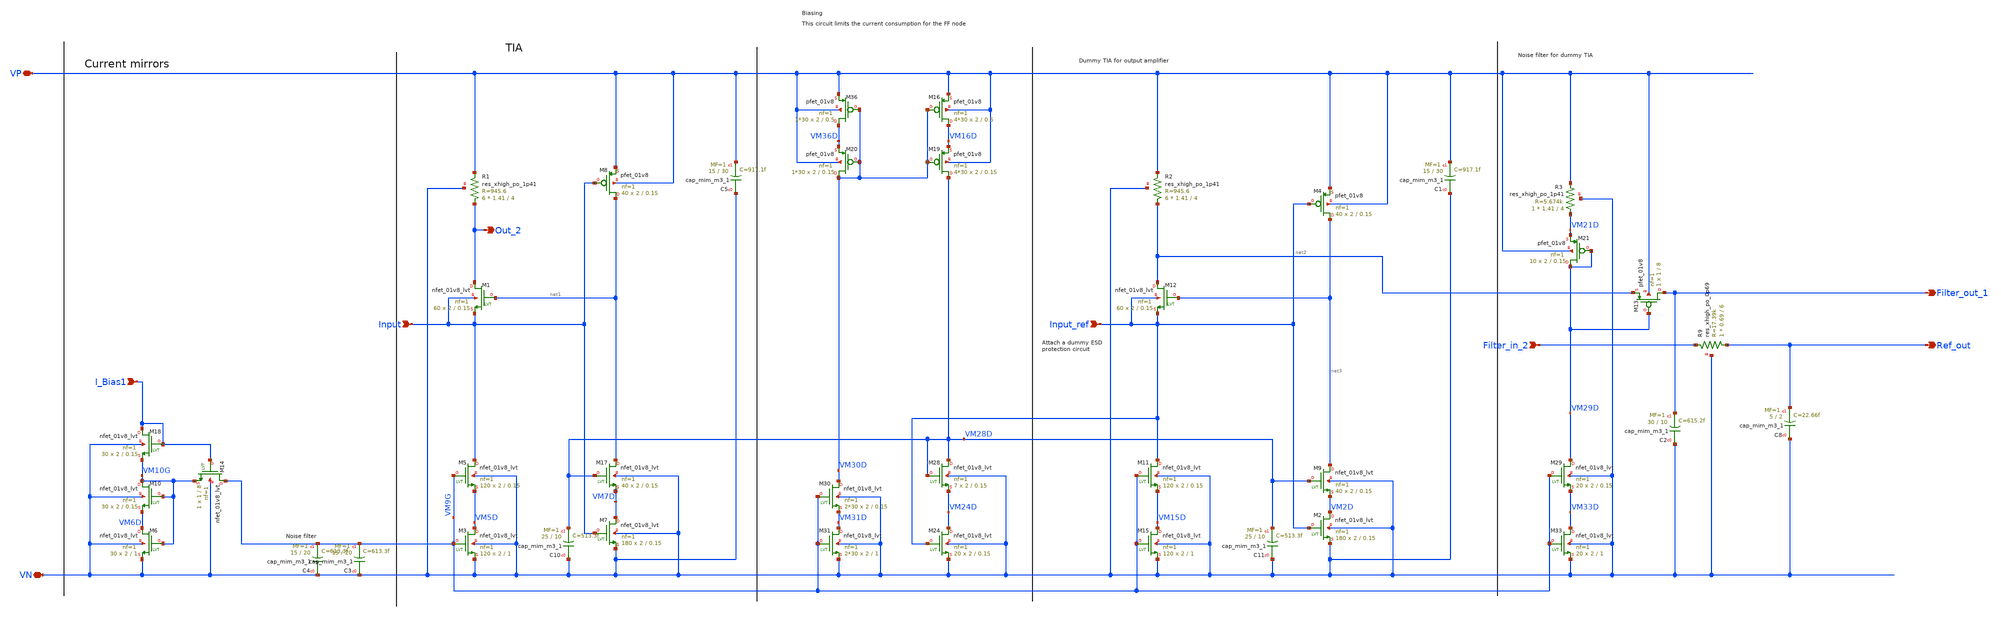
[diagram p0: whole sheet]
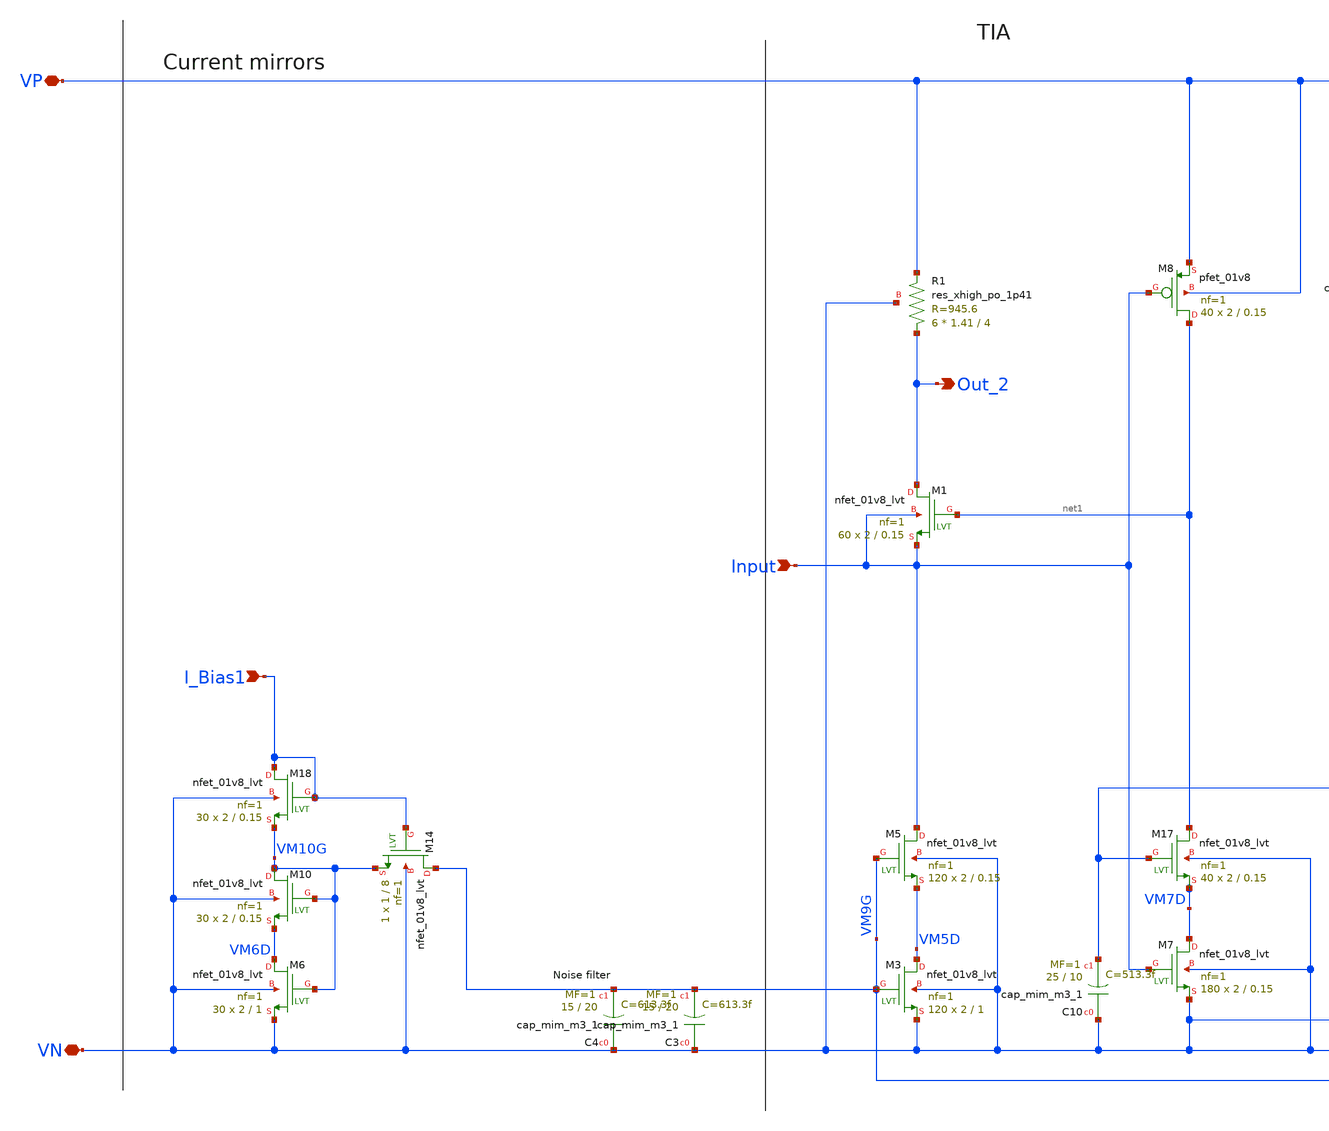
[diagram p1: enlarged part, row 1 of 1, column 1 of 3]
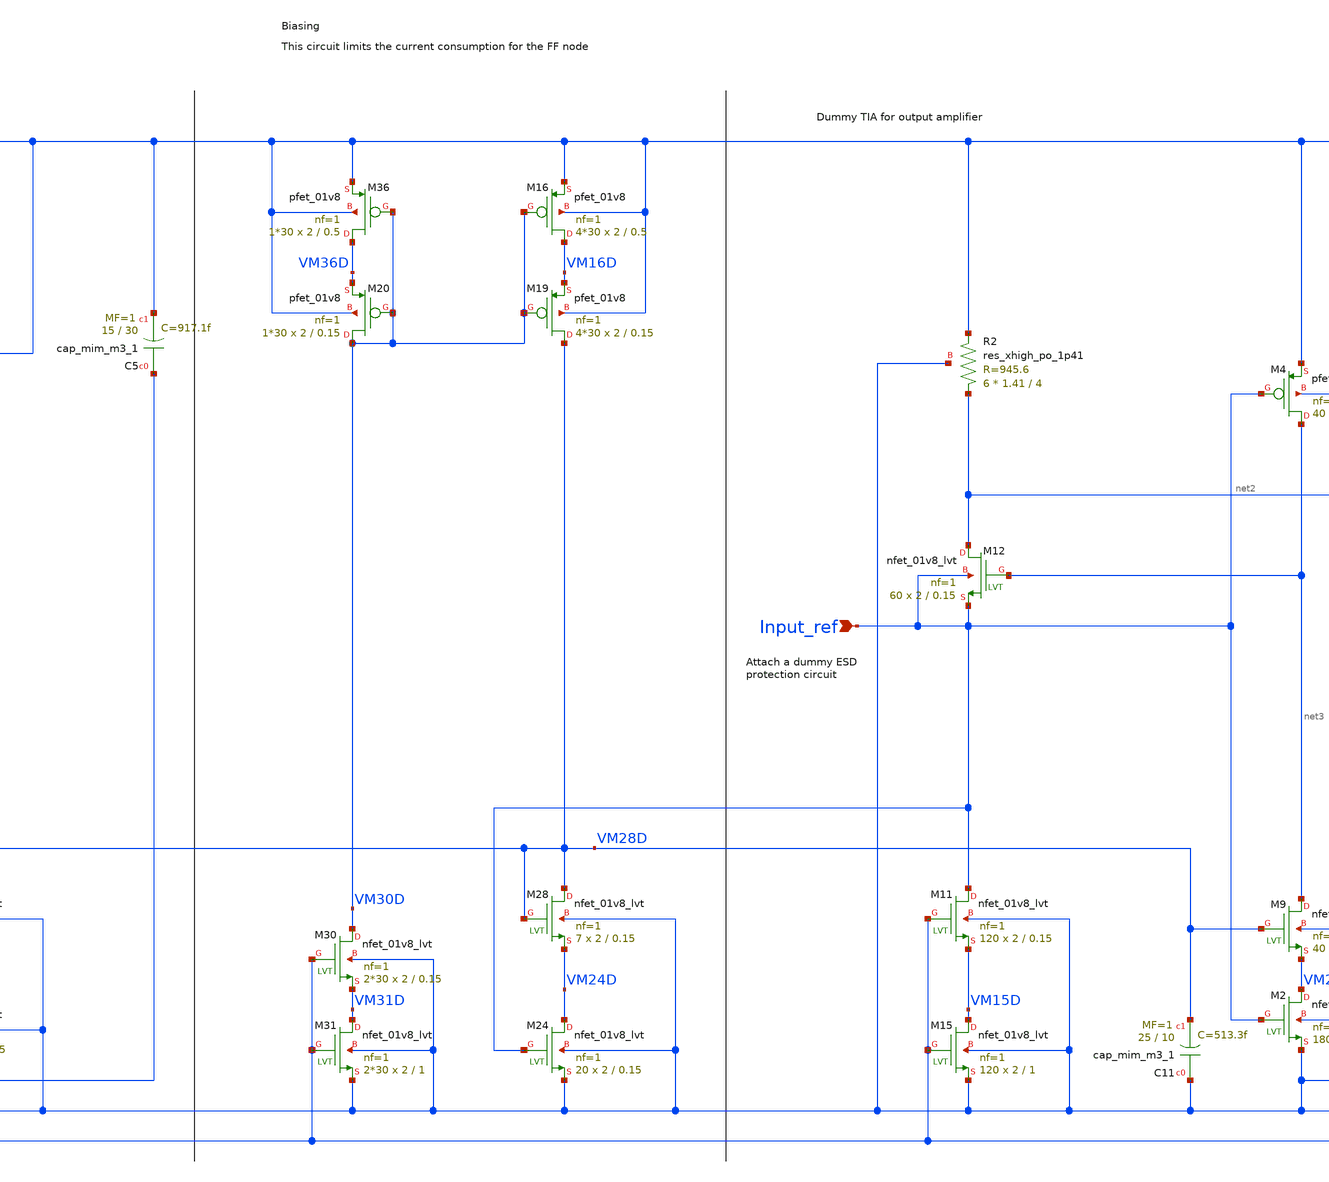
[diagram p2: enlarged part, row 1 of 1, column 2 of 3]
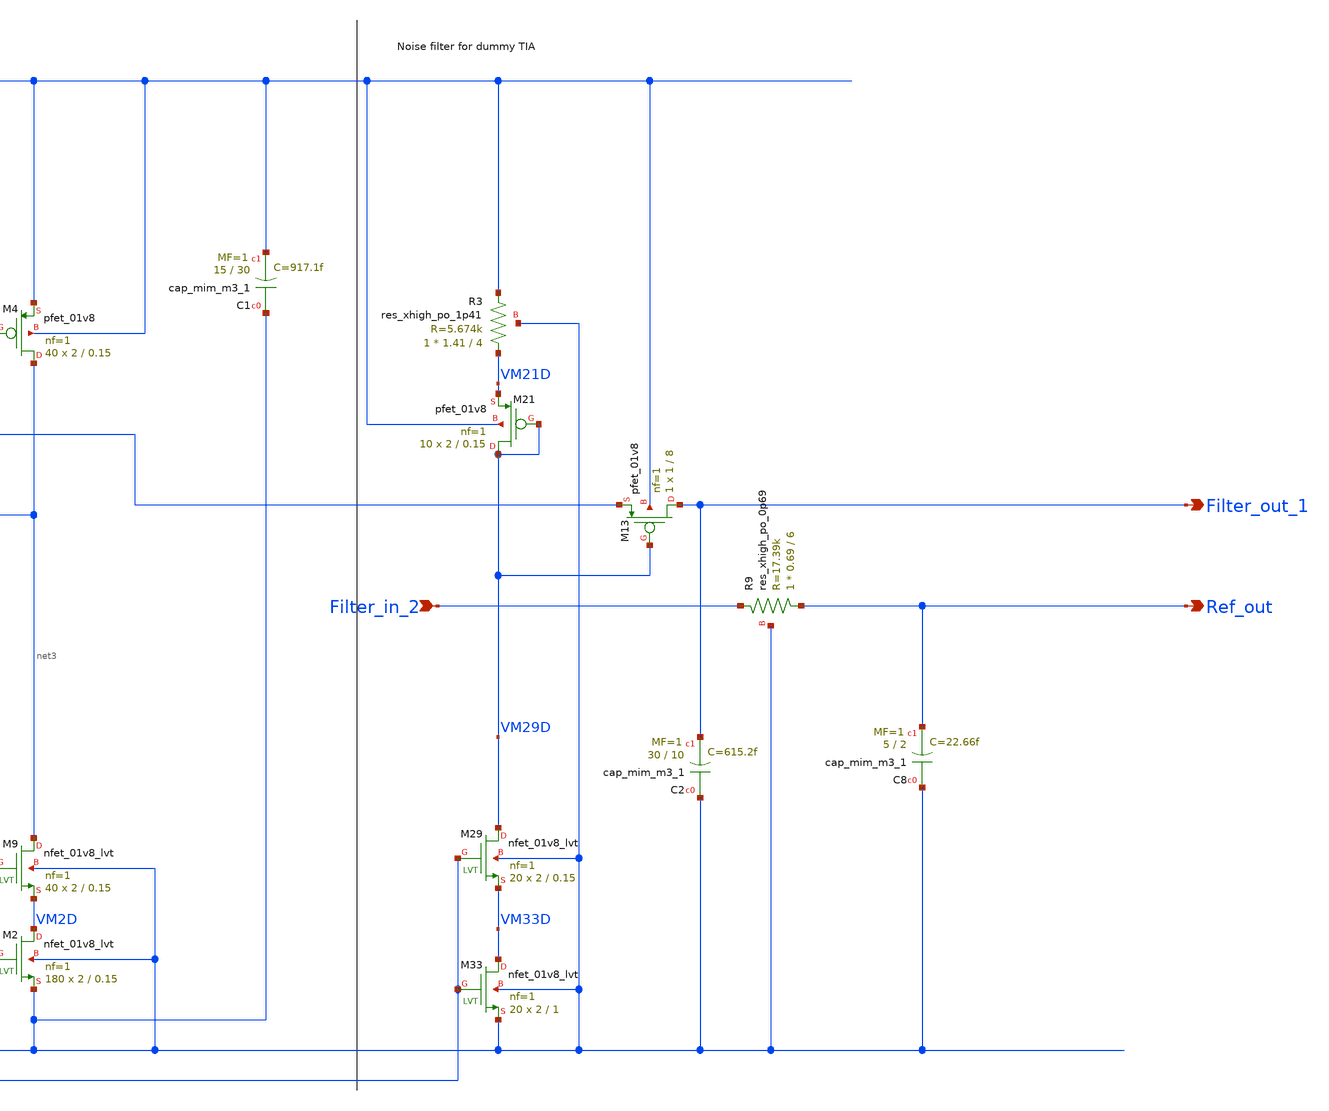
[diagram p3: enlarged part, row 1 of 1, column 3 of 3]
** sch_path: xschem/tia/tiaA.sch
**.subckt tiaA VN VP Out_2 I_Bias1 Input Input_ref Filter_out_1 Filter_in_2 Ref_out
*.iopin VN
*.iopin VP
*.opin Out_2
*.ipin I_Bias1
*.ipin Input
*.ipin Input_ref
*.opin Filter_out_1
*.ipin Filter_in_2
*.opin Ref_out
XM7 VM7D Input VN VN sky130_fd_pr__nfet_01v8_lvt L=0.15 W=2 nf=1 ad='int((nf+1)/2) * W/nf * 0.29' as='int((nf+2)/2) * W/nf * 0.29'
+ pd='2*int((nf+1)/2) * (W/nf + 0.29)' ps='2*int((nf+2)/2) * (W/nf + 0.29)' nrd='0.29 / W' nrs='0.29 / W'
+ sa=0 sb=0 sd=0 mult=180 m=180
XM8 net1 Input VP VP sky130_fd_pr__pfet_01v8 L=0.15 W=2 nf=1 ad='int((nf+1)/2) * W/nf * 0.29' as='int((nf+2)/2) * W/nf * 0.29'
+ pd='2*int((nf+1)/2) * (W/nf + 0.29)' ps='2*int((nf+2)/2) * (W/nf + 0.29)' nrd='0.29 / W' nrs='0.29 / W'
+ sa=0 sb=0 sd=0 mult=40 m=40
XC4 VN VM9G sky130_fd_pr__cap_mim_m3_1 W=15 L=20 MF=1 m=1
XM18 I_Bias1 I_Bias1 VM10G VN sky130_fd_pr__nfet_01v8_lvt L=0.15 W=2 nf=1 ad='int((nf+1)/2) * W/nf * 0.29'
+ as='int((nf+2)/2) * W/nf * 0.29' pd='2*int((nf+1)/2) * (W/nf + 0.29)' ps='2*int((nf+2)/2) * (W/nf + 0.29)'
+ nrd='0.29 / W' nrs='0.29 / W' sa=0 sb=0 sd=0 mult=30 m=30
XM10 VM10G VM10G VM6D VN sky130_fd_pr__nfet_01v8_lvt L=0.15 W=2 nf=1 ad='int((nf+1)/2) * W/nf * 0.29'
+ as='int((nf+2)/2) * W/nf * 0.29' pd='2*int((nf+1)/2) * (W/nf + 0.29)' ps='2*int((nf+2)/2) * (W/nf + 0.29)'
+ nrd='0.29 / W' nrs='0.29 / W' sa=0 sb=0 sd=0 mult=30 m=30
XM5 Input VM9G VM5D VN sky130_fd_pr__nfet_01v8_lvt L=0.15 W=2 nf=1 ad='int((nf+1)/2) * W/nf * 0.29' as='int((nf+2)/2) * W/nf * 0.29'
+ pd='2*int((nf+1)/2) * (W/nf + 0.29)' ps='2*int((nf+2)/2) * (W/nf + 0.29)' nrd='0.29 / W' nrs='0.29 / W'
+ sa=0 sb=0 sd=0 mult=120 m=120
XM6 VM6D VM10G VN VN sky130_fd_pr__nfet_01v8_lvt L=1 W=2 nf=1 ad='int((nf+1)/2) * W/nf * 0.29' as='int((nf+2)/2) * W/nf * 0.29'
+ pd='2*int((nf+1)/2) * (W/nf + 0.29)' ps='2*int((nf+2)/2) * (W/nf + 0.29)' nrd='0.29 / W' nrs='0.29 / W'
+ sa=0 sb=0 sd=0 mult=30 m=30
XM14 VM9G I_Bias1 VM10G VN sky130_fd_pr__nfet_01v8_lvt L=8 W=1 nf=1 ad='int((nf+1)/2) * W/nf * 0.29'
+ as='int((nf+2)/2) * W/nf * 0.29' pd='2*int((nf+1)/2) * (W/nf + 0.29)' ps='2*int((nf+2)/2) * (W/nf + 0.29)'
+ nrd='0.29 / W' nrs='0.29 / W' sa=0 sb=0 sd=0 mult=1 m=1
XM1 Out_2 net1 Input Input sky130_fd_pr__nfet_01v8_lvt L=0.15 W=2 nf=1 ad='int((nf+1)/2) * W/nf * 0.29'
+ as='int((nf+2)/2) * W/nf * 0.29' pd='2*int((nf+1)/2) * (W/nf + 0.29)' ps='2*int((nf+2)/2) * (W/nf + 0.29)'
+ nrd='0.29 / W' nrs='0.29 / W' sa=0 sb=0 sd=0 mult=60 m=60
XM3 VM5D VM9G VN VN sky130_fd_pr__nfet_01v8_lvt L=1 W=2 nf=1 ad='int((nf+1)/2) * W/nf * 0.29' as='int((nf+2)/2) * W/nf * 0.29'
+ pd='2*int((nf+1)/2) * (W/nf + 0.29)' ps='2*int((nf+2)/2) * (W/nf + 0.29)' nrd='0.29 / W' nrs='0.29 / W'
+ sa=0 sb=0 sd=0 mult=120 m=120
XR1 Out_2 VP VN sky130_fd_pr__res_xhigh_po_1p41 L=4 mult=6 m=6
XM2 VM2D Input_ref VN VN sky130_fd_pr__nfet_01v8_lvt L=0.15 W=2 nf=1 ad='int((nf+1)/2) * W/nf * 0.29'
+ as='int((nf+2)/2) * W/nf * 0.29' pd='2*int((nf+1)/2) * (W/nf + 0.29)' ps='2*int((nf+2)/2) * (W/nf + 0.29)'
+ nrd='0.29 / W' nrs='0.29 / W' sa=0 sb=0 sd=0 mult=180 m=180
XM4 net3 Input_ref VP VP sky130_fd_pr__pfet_01v8 L=0.15 W=2 nf=1 ad='int((nf+1)/2) * W/nf * 0.29' as='int((nf+2)/2) * W/nf * 0.29'
+ pd='2*int((nf+1)/2) * (W/nf + 0.29)' ps='2*int((nf+2)/2) * (W/nf + 0.29)' nrd='0.29 / W' nrs='0.29 / W'
+ sa=0 sb=0 sd=0 mult=40 m=40
XM11 Input_ref VM9G VM15D VN sky130_fd_pr__nfet_01v8_lvt L=0.15 W=2 nf=1 ad='int((nf+1)/2) * W/nf * 0.29'
+ as='int((nf+2)/2) * W/nf * 0.29' pd='2*int((nf+1)/2) * (W/nf + 0.29)' ps='2*int((nf+2)/2) * (W/nf + 0.29)'
+ nrd='0.29 / W' nrs='0.29 / W' sa=0 sb=0 sd=0 mult=120 m=120
XM12 net2 net3 Input_ref Input_ref sky130_fd_pr__nfet_01v8_lvt L=0.15 W=2 nf=1 ad='int((nf+1)/2) * W/nf * 0.29'
+ as='int((nf+2)/2) * W/nf * 0.29' pd='2*int((nf+1)/2) * (W/nf + 0.29)' ps='2*int((nf+2)/2) * (W/nf + 0.29)'
+ nrd='0.29 / W' nrs='0.29 / W' sa=0 sb=0 sd=0 mult=60 m=60
XM15 VM15D VM9G VN VN sky130_fd_pr__nfet_01v8_lvt L=1 W=2 nf=1 ad='int((nf+1)/2) * W/nf * 0.29' as='int((nf+2)/2) * W/nf * 0.29'
+ pd='2*int((nf+1)/2) * (W/nf + 0.29)' ps='2*int((nf+2)/2) * (W/nf + 0.29)' nrd='0.29 / W' nrs='0.29 / W'
+ sa=0 sb=0 sd=0 mult=120 m=120
XR2 net2 VP VN sky130_fd_pr__res_xhigh_po_1p41 L=4 mult=6 m=6
XC5 VN VP sky130_fd_pr__cap_mim_m3_1 W=15 L=30 MF=1 m=1
XC1 VN VP sky130_fd_pr__cap_mim_m3_1 W=15 L=30 MF=1 m=1
XC2 VN Filter_out_1 sky130_fd_pr__cap_mim_m3_1 W=30 L=10 MF=1 m=1
XM29 VM29D VM9G VM33D VN sky130_fd_pr__nfet_01v8_lvt L=0.15 W=2 nf=1 ad='int((nf+1)/2) * W/nf * 0.29'
+ as='int((nf+2)/2) * W/nf * 0.29' pd='2*int((nf+1)/2) * (W/nf + 0.29)' ps='2*int((nf+2)/2) * (W/nf + 0.29)'
+ nrd='0.29 / W' nrs='0.29 / W' sa=0 sb=0 sd=0 mult=20 m=20
XM33 VM33D VM9G VN VN sky130_fd_pr__nfet_01v8_lvt L=1 W=2 nf=1 ad='int((nf+1)/2) * W/nf * 0.29' as='int((nf+2)/2) * W/nf * 0.29'
+ pd='2*int((nf+1)/2) * (W/nf + 0.29)' ps='2*int((nf+2)/2) * (W/nf + 0.29)' nrd='0.29 / W' nrs='0.29 / W'
+ sa=0 sb=0 sd=0 mult=20 m=20
XR3 VM21D VP VN sky130_fd_pr__res_xhigh_po_1p41 L=4 mult=1 m=1
XM21 VM29D VM29D VM21D VP sky130_fd_pr__pfet_01v8 L=0.15 W=2 nf=1 ad='int((nf+1)/2) * W/nf * 0.29' as='int((nf+2)/2) * W/nf * 0.29'
+ pd='2*int((nf+1)/2) * (W/nf + 0.29)' ps='2*int((nf+2)/2) * (W/nf + 0.29)' nrd='0.29 / W' nrs='0.29 / W'
+ sa=0 sb=0 sd=0 mult=10 m=10
XM13 Filter_out_1 VM29D net2 VP sky130_fd_pr__pfet_01v8 L=8 W=1 nf=1 ad='int((nf+1)/2) * W/nf * 0.29'
+ as='int((nf+2)/2) * W/nf * 0.29' pd='2*int((nf+1)/2) * (W/nf + 0.29)' ps='2*int((nf+2)/2) * (W/nf + 0.29)'
+ nrd='0.29 / W' nrs='0.29 / W' sa=0 sb=0 sd=0 mult=1 m=1
XM24 VM24D Input_ref VN VN sky130_fd_pr__nfet_01v8_lvt L=0.15 W=2 nf=1 ad='int((nf+1)/2) * W/nf * 0.29'
+ as='int((nf+2)/2) * W/nf * 0.29' pd='2*int((nf+1)/2) * (W/nf + 0.29)' ps='2*int((nf+2)/2) * (W/nf + 0.29)'
+ nrd='0.29 / W' nrs='0.29 / W' sa=0 sb=0 sd=0 mult=20 m=20
XM30 VM30D VM9G VM31D VN sky130_fd_pr__nfet_01v8_lvt L=0.15 W=2 nf=1 ad='int((nf+1)/2) * W/nf * 0.29'
+ as='int((nf+2)/2) * W/nf * 0.29' pd='2*int((nf+1)/2) * (W/nf + 0.29)' ps='2*int((nf+2)/2) * (W/nf + 0.29)'
+ nrd='0.29 / W' nrs='0.29 / W' sa=0 sb=0 sd=0 mult=2*30 m=2*30
XM31 VM31D VM9G VN VN sky130_fd_pr__nfet_01v8_lvt L=1 W=2 nf=1 ad='int((nf+1)/2) * W/nf * 0.29' as='int((nf+2)/2) * W/nf * 0.29'
+ pd='2*int((nf+1)/2) * (W/nf + 0.29)' ps='2*int((nf+2)/2) * (W/nf + 0.29)' nrd='0.29 / W' nrs='0.29 / W'
+ sa=0 sb=0 sd=0 mult=2*30 m=2*30
XM28 VM28D VM28D VM24D VN sky130_fd_pr__nfet_01v8_lvt L=0.15 W=2 nf=1 ad='int((nf+1)/2) * W/nf * 0.29'
+ as='int((nf+2)/2) * W/nf * 0.29' pd='2*int((nf+1)/2) * (W/nf + 0.29)' ps='2*int((nf+2)/2) * (W/nf + 0.29)'
+ nrd='0.29 / W' nrs='0.29 / W' sa=0 sb=0 sd=0 mult=7 m=7
XM17 net1 VM28D VM7D VN sky130_fd_pr__nfet_01v8_lvt L=0.15 W=2 nf=1 ad='int((nf+1)/2) * W/nf * 0.29'
+ as='int((nf+2)/2) * W/nf * 0.29' pd='2*int((nf+1)/2) * (W/nf + 0.29)' ps='2*int((nf+2)/2) * (W/nf + 0.29)'
+ nrd='0.29 / W' nrs='0.29 / W' sa=0 sb=0 sd=0 mult=40 m=40
XM9 net3 VM28D VM2D VN sky130_fd_pr__nfet_01v8_lvt L=0.15 W=2 nf=1 ad='int((nf+1)/2) * W/nf * 0.29' as='int((nf+2)/2) * W/nf * 0.29'
+ pd='2*int((nf+1)/2) * (W/nf + 0.29)' ps='2*int((nf+2)/2) * (W/nf + 0.29)' nrd='0.29 / W' nrs='0.29 / W'
+ sa=0 sb=0 sd=0 mult=40 m=40
XC10 VN VM28D sky130_fd_pr__cap_mim_m3_1 W=25 L=10 MF=1 m=1
XC11 VN VM28D sky130_fd_pr__cap_mim_m3_1 W=25 L=10 MF=1 m=1
XM36 VM36D VM30D VP VP sky130_fd_pr__pfet_01v8 L=0.5 W=2 nf=1 ad='int((nf+1)/2) * W/nf * 0.29' as='int((nf+2)/2) * W/nf * 0.29'
+ pd='2*int((nf+1)/2) * (W/nf + 0.29)' ps='2*int((nf+2)/2) * (W/nf + 0.29)' nrd='0.29 / W' nrs='0.29 / W'
+ sa=0 sb=0 sd=0 mult=1*30 m=1*30
XM16 VM16D VM30D VP VP sky130_fd_pr__pfet_01v8 L=0.5 W=2 nf=1 ad='int((nf+1)/2) * W/nf * 0.29' as='int((nf+2)/2) * W/nf * 0.29'
+ pd='2*int((nf+1)/2) * (W/nf + 0.29)' ps='2*int((nf+2)/2) * (W/nf + 0.29)' nrd='0.29 / W' nrs='0.29 / W'
+ sa=0 sb=0 sd=0 mult=4*30 m=4*30
XM19 VM28D VM30D VM16D VP sky130_fd_pr__pfet_01v8 L=0.15 W=2 nf=1 ad='int((nf+1)/2) * W/nf * 0.29' as='int((nf+2)/2) * W/nf * 0.29'
+ pd='2*int((nf+1)/2) * (W/nf + 0.29)' ps='2*int((nf+2)/2) * (W/nf + 0.29)' nrd='0.29 / W' nrs='0.29 / W'
+ sa=0 sb=0 sd=0 mult=4*30 m=4*30
XM20 VM30D VM30D VM36D VP sky130_fd_pr__pfet_01v8 L=0.15 W=2 nf=1 ad='int((nf+1)/2) * W/nf * 0.29' as='int((nf+2)/2) * W/nf * 0.29'
+ pd='2*int((nf+1)/2) * (W/nf + 0.29)' ps='2*int((nf+2)/2) * (W/nf + 0.29)' nrd='0.29 / W' nrs='0.29 / W'
+ sa=0 sb=0 sd=0 mult=1*30 m=1*30
XC8 VN Ref_out sky130_fd_pr__cap_mim_m3_1 W=5 L=2 MF=1 m=1
XR9 Ref_out Filter_in_2 VN sky130_fd_pr__res_xhigh_po_0p69 L=6 mult=1 m=1
XC3 VN VM9G sky130_fd_pr__cap_mim_m3_1 W=15 L=20 MF=1 m=1
**.ends
.end
